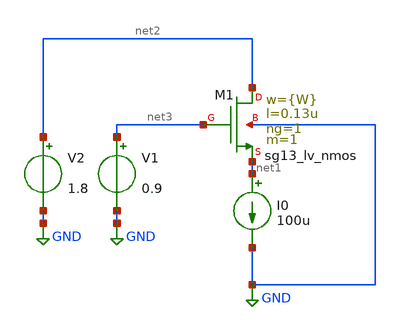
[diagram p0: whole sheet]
** sch_path: xschem/TB/gm_vs_W.sch
**.subckt gm_vs_W
XM1 net2 net3 net1 GND sg13_lv_nmos w={W} l=0.13u ng=1 m=1 mm_ok=1
I0 net1 GND 100u
V1 net3 GND 0.9
V2 net2 GND 1.8
**** begin user architecture code


.param W = 1.0u
.control
let strt_w = 1.0u
let stop_w = 10u
let step_w = 0.1u
let curr_w = 1.0u
save all
while curr_w le stop_w
	alterparam W = $&curr_w
	reset
	save all
	+ @n.xm1.nsg13_lv_nmos[gm]
	op
	let gmn = @n.xm1.nsg13_lv_nmos[gm]
	wrdata ../proyecto-IPD413/simulations/gm_vs_w.raw gmn curr_w
	set appendwrite
	let curr_w = curr_w + step_w
end
.endc




.lib cornerMOSlv.lib mos_tt


**** end user architecture code
**.ends
.GLOBAL GND
.end
